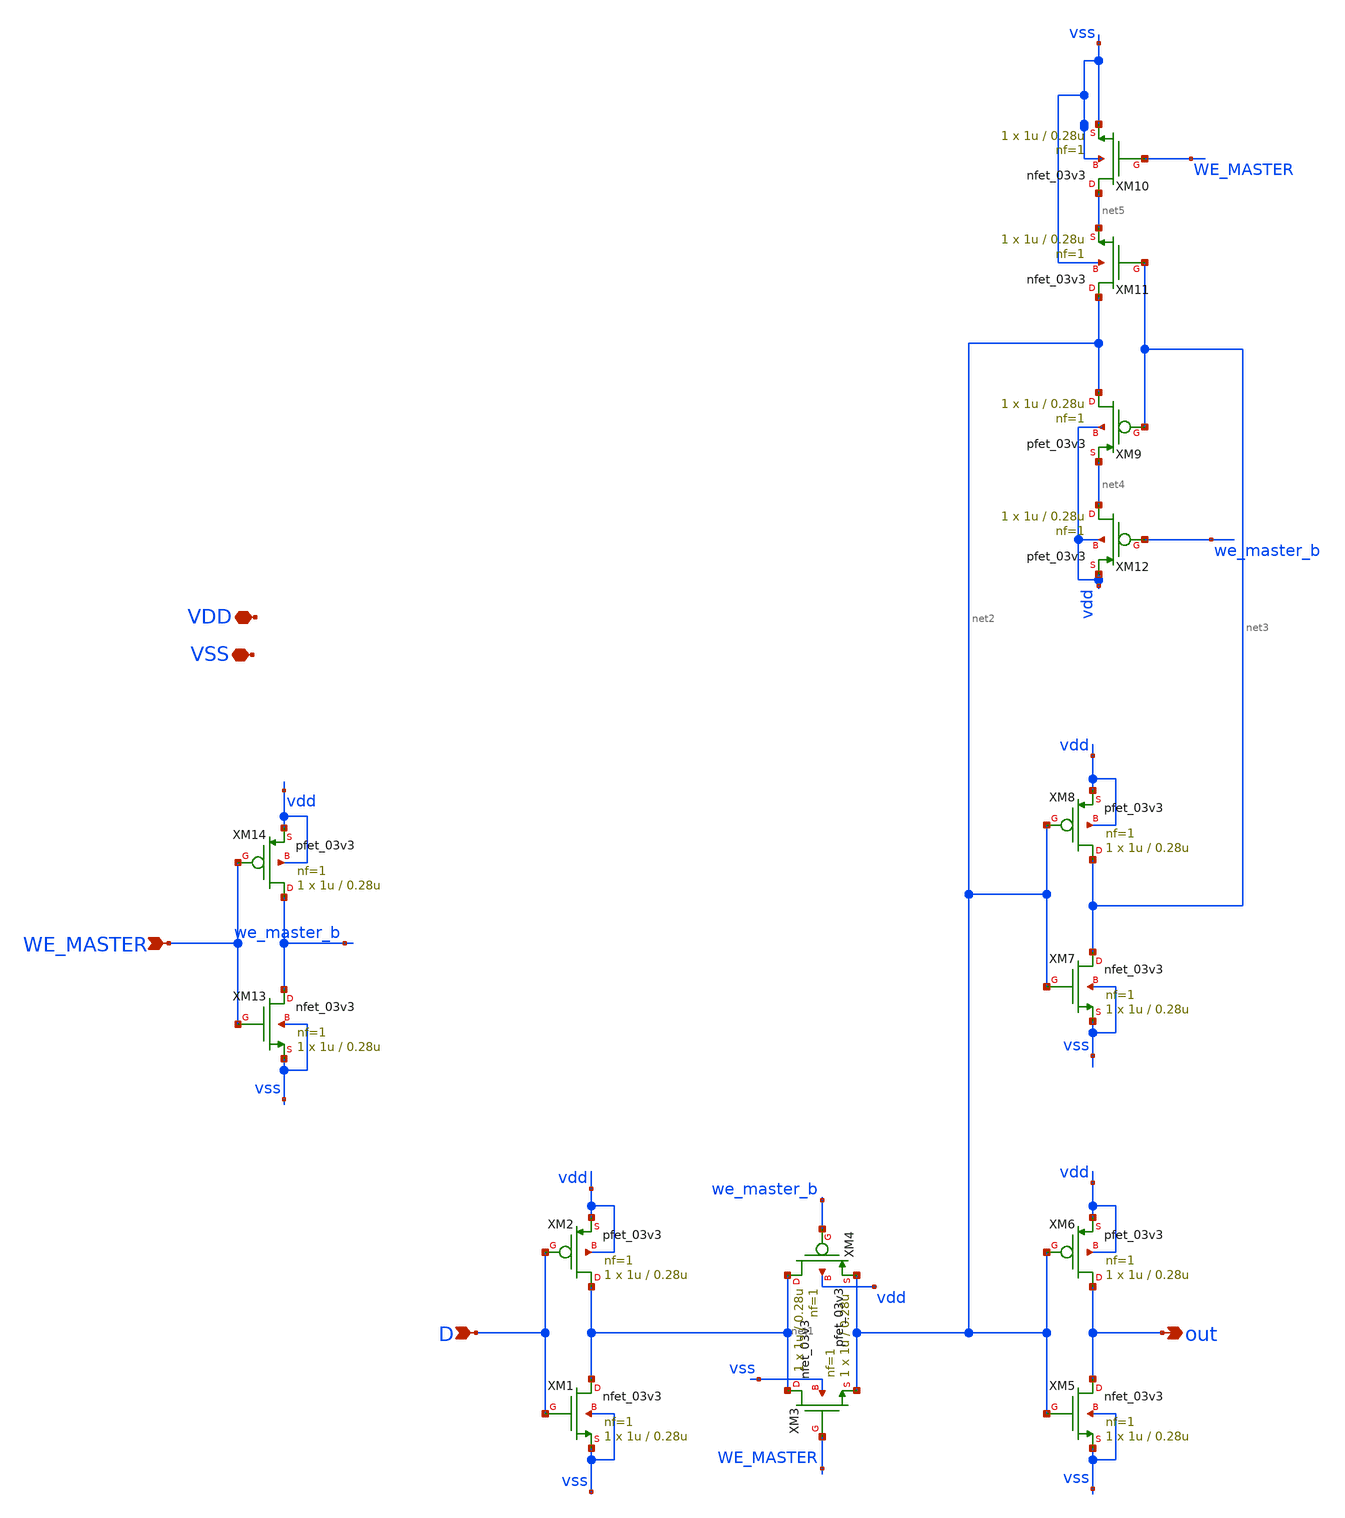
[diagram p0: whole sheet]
** sch_path: CAD3/master_latch.sch
**.subckt master_latch D VDD VSS WE_MASTER out
*.ipin D
*.iopin VDD
*.iopin VSS
*.ipin WE_MASTER
*.opin out
XM1 net1 D vss vss nfet_03v3 L=0.28u W=1u nf=1 ad='int((nf+1)/2) * W/nf * 0.18u' as='int((nf+2)/2) * W/nf * 0.18u'
+ pd='2*int((nf+1)/2) * (W/nf + 0.18u)' ps='2*int((nf+2)/2) * (W/nf + 0.18u)' nrd='0.18u / W' nrs='0.18u / W'
+ sa=0 sb=0 sd=0 m=1
XM2 net1 D vdd vdd pfet_03v3 L=0.28u W=1u nf=1 ad='int((nf+1)/2) * W/nf * 0.18u' as='int((nf+2)/2) * W/nf * 0.18u'
+ pd='2*int((nf+1)/2) * (W/nf + 0.18u)' ps='2*int((nf+2)/2) * (W/nf + 0.18u)' nrd='0.18u / W' nrs='0.18u / W'
+ sa=0 sb=0 sd=0 m=1
XM3 net6 WE_MASTER net2 vss nfet_03v3 L=0.28u W=1u nf=1 ad='int((nf+1)/2) * W/nf * 0.18u' as='int((nf+2)/2) * W/nf * 0.18u'
+ pd='2*int((nf+1)/2) * (W/nf + 0.18u)' ps='2*int((nf+2)/2) * (W/nf + 0.18u)' nrd='0.18u / W' nrs='0.18u / W'
+ sa=0 sb=0 sd=0 m=1
XM4 net1 we_master_b net2 vdd pfet_03v3 L=0.28u W=1u nf=1 ad='int((nf+1)/2) * W/nf * 0.18u' as='int((nf+2)/2) * W/nf * 0.18u'
+ pd='2*int((nf+1)/2) * (W/nf + 0.18u)' ps='2*int((nf+2)/2) * (W/nf + 0.18u)' nrd='0.18u / W' nrs='0.18u / W'
+ sa=0 sb=0 sd=0 m=1
XM5 out net2 vss vss nfet_03v3 L=0.28u W=1u nf=1 ad='int((nf+1)/2) * W/nf * 0.18u' as='int((nf+2)/2) * W/nf * 0.18u'
+ pd='2*int((nf+1)/2) * (W/nf + 0.18u)' ps='2*int((nf+2)/2) * (W/nf + 0.18u)' nrd='0.18u / W' nrs='0.18u / W'
+ sa=0 sb=0 sd=0 m=1
XM6 out net2 vdd vdd pfet_03v3 L=0.28u W=1u nf=1 ad='int((nf+1)/2) * W/nf * 0.18u' as='int((nf+2)/2) * W/nf * 0.18u'
+ pd='2*int((nf+1)/2) * (W/nf + 0.18u)' ps='2*int((nf+2)/2) * (W/nf + 0.18u)' nrd='0.18u / W' nrs='0.18u / W'
+ sa=0 sb=0 sd=0 m=1
XM7 net3 net2 vss vss nfet_03v3 L=0.28u W=1u nf=1 ad='int((nf+1)/2) * W/nf * 0.18u' as='int((nf+2)/2) * W/nf * 0.18u'
+ pd='2*int((nf+1)/2) * (W/nf + 0.18u)' ps='2*int((nf+2)/2) * (W/nf + 0.18u)' nrd='0.18u / W' nrs='0.18u / W'
+ sa=0 sb=0 sd=0 m=1
XM8 net3 net2 vdd vdd pfet_03v3 L=0.28u W=1u nf=1 ad='int((nf+1)/2) * W/nf * 0.18u' as='int((nf+2)/2) * W/nf * 0.18u'
+ pd='2*int((nf+1)/2) * (W/nf + 0.18u)' ps='2*int((nf+2)/2) * (W/nf + 0.18u)' nrd='0.18u / W' nrs='0.18u / W'
+ sa=0 sb=0 sd=0 m=1
XM9 net2 net3 net4 vdd pfet_03v3 L=0.28u W=1u nf=1 ad='int((nf+1)/2) * W/nf * 0.18u' as='int((nf+2)/2) * W/nf * 0.18u'
+ pd='2*int((nf+1)/2) * (W/nf + 0.18u)' ps='2*int((nf+2)/2) * (W/nf + 0.18u)' nrd='0.18u / W' nrs='0.18u / W'
+ sa=0 sb=0 sd=0 m=1
XM10 net5 WE_MASTER vss vss nfet_03v3 L=0.28u W=1u nf=1 ad='int((nf+1)/2) * W/nf * 0.18u' as='int((nf+2)/2) * W/nf * 0.18u'
+ pd='2*int((nf+1)/2) * (W/nf + 0.18u)' ps='2*int((nf+2)/2) * (W/nf + 0.18u)' nrd='0.18u / W' nrs='0.18u / W'
+ sa=0 sb=0 sd=0 m=1
XM11 net2 net3 net5 vss nfet_03v3 L=0.28u W=1u nf=1 ad='int((nf+1)/2) * W/nf * 0.18u' as='int((nf+2)/2) * W/nf * 0.18u'
+ pd='2*int((nf+1)/2) * (W/nf + 0.18u)' ps='2*int((nf+2)/2) * (W/nf + 0.18u)' nrd='0.18u / W' nrs='0.18u / W'
+ sa=0 sb=0 sd=0 m=1
XM12 net4 we_master_b vdd vdd pfet_03v3 L=0.28u W=1u nf=1 ad='int((nf+1)/2) * W/nf * 0.18u' as='int((nf+2)/2) * W/nf * 0.18u'
+ pd='2*int((nf+1)/2) * (W/nf + 0.18u)' ps='2*int((nf+2)/2) * (W/nf + 0.18u)' nrd='0.18u / W' nrs='0.18u / W'
+ sa=0 sb=0 sd=0 m=1
XM13 we_master_b WE_MASTER vss vss nfet_03v3 L=0.28u W=1u nf=1 ad='int((nf+1)/2) * W/nf * 0.18u' as='int((nf+2)/2) * W/nf * 0.18u'
+ pd='2*int((nf+1)/2) * (W/nf + 0.18u)' ps='2*int((nf+2)/2) * (W/nf + 0.18u)' nrd='0.18u / W' nrs='0.18u / W'
+ sa=0 sb=0 sd=0 m=1
XM14 we_master_b WE_MASTER vdd vdd pfet_03v3 L=0.28u W=1u nf=1 ad='int((nf+1)/2) * W/nf * 0.18u' as='int((nf+2)/2) * W/nf * 0.18u'
+ pd='2*int((nf+1)/2) * (W/nf + 0.18u)' ps='2*int((nf+2)/2) * (W/nf + 0.18u)' nrd='0.18u / W' nrs='0.18u / W'
+ sa=0 sb=0 sd=0 m=1
**.ends
.end
